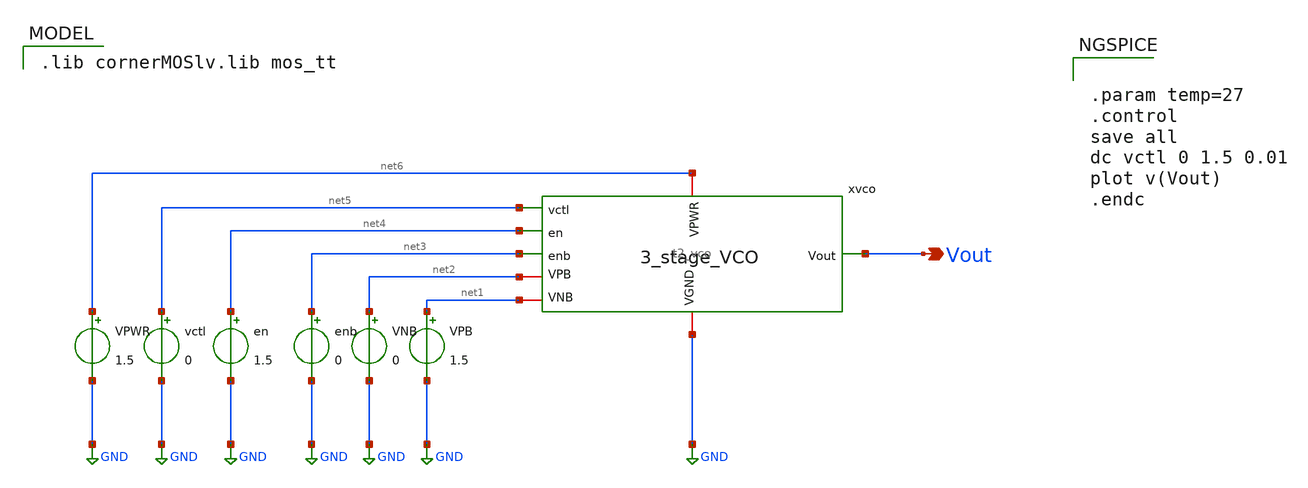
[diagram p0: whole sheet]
** sch_path: Team 2 Design/design_data/xschem/t2_vco_tb.sch
**.subckt t2_vco_tb Vout
*.opin Vout
x1 net6 net2 GND net1 Vout net5 net4 net3 t2_vco
VPWR net6 GND 1.5
vctl net5 GND 0
en net4 GND 1.5
enb net3 GND 0
VNB net2 GND 0
VPB net1 GND 1.5
**** begin user architecture code
 .lib cornerMOSlv.lib mos_tt



.param temp=27
.control
save all
dc vctl 0 1.5 0.01
plot v(Vout)
.endc


**** end user architecture code
**.ends
.GLOBAL GND
.end
